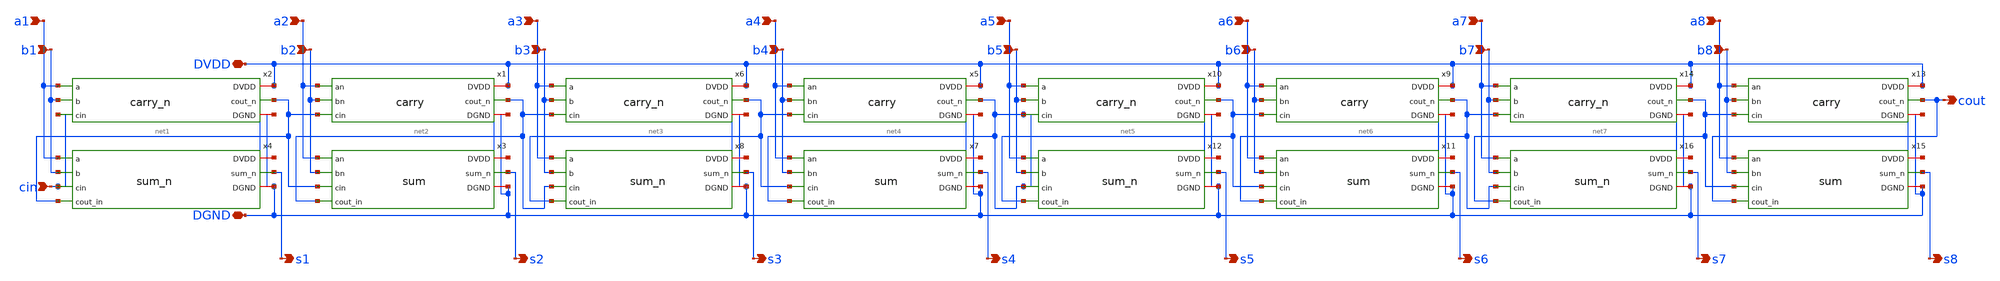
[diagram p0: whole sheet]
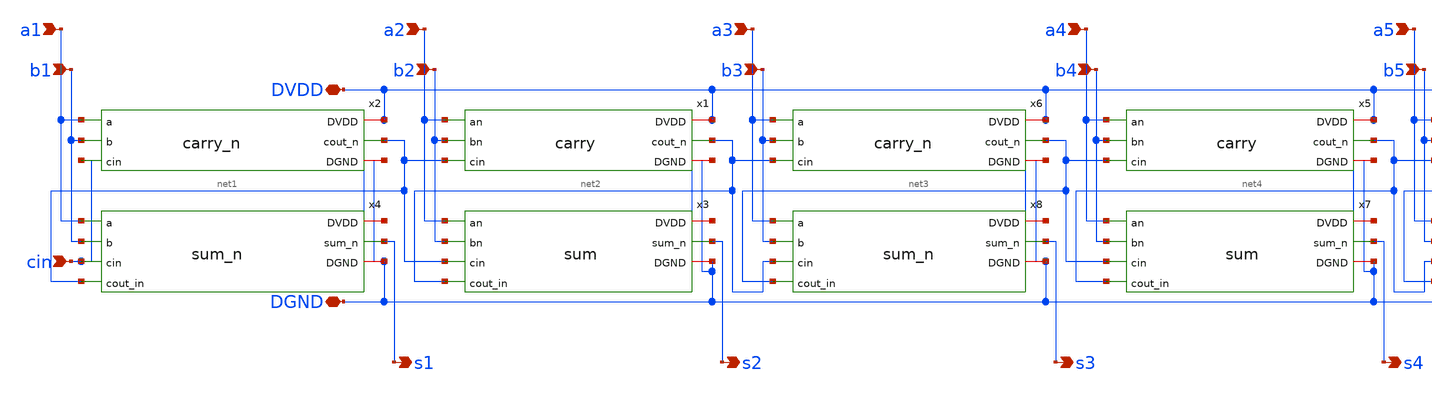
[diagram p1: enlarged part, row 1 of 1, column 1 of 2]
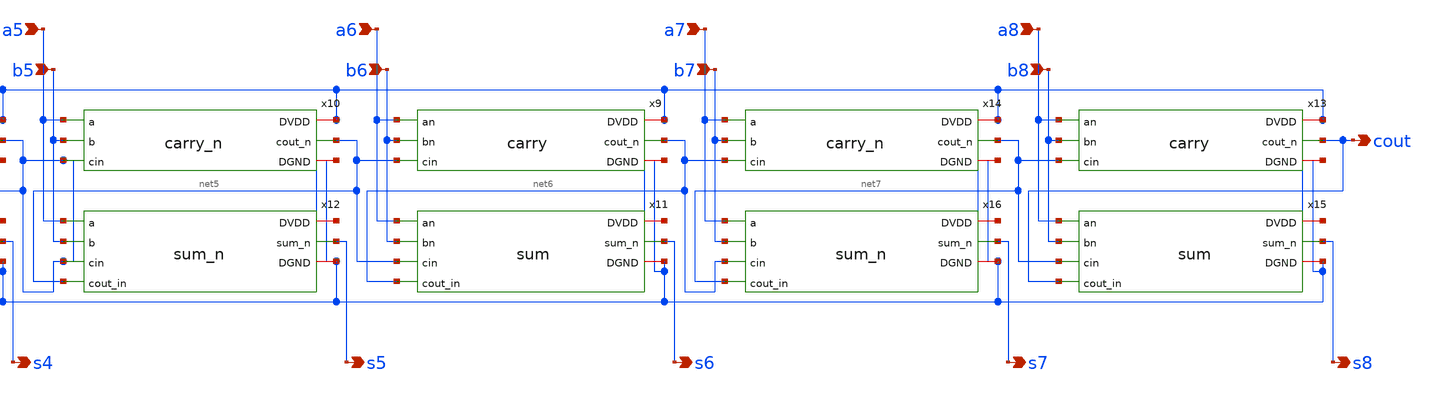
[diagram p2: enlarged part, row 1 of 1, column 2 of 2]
** sch_path: tut6/rca/rca8b.sch
**.subckt rca8b cin a1 b1 a2 b2 a3 b3 a4 b4 a5 b5 a6 b6 a7 b7 a8 b8 DVDD DGND s1 s2 s3 s4 s5 s6 s7
*+ s8 cout
*.ipin cin
*.ipin a1
*.ipin b1
*.ipin a2
*.ipin b2
*.ipin a3
*.ipin b3
*.ipin a4
*.ipin b4
*.ipin a5
*.ipin b5
*.ipin a6
*.ipin b6
*.ipin a7
*.ipin b7
*.ipin a8
*.ipin b8
*.iopin DVDD
*.iopin DGND
*.opin s1
*.opin s2
*.opin s3
*.opin s4
*.opin s5
*.opin s6
*.opin s7
*.opin s8
*.opin cout
x1 DVDD a2 b2 net2 net1 DGND carry
x2 DVDD a1 b1 net1 cin DGND carry_n
x3 DVDD a2 s2 b2 net1 net2 DGND sum
x4 DVDD a1 b1 s1 cin net1 DGND sum_n
x5 DVDD a4 b4 net4 net3 DGND carry
x6 DVDD a3 b3 net3 net2 DGND carry_n
x7 DVDD a4 s4 b4 net3 net4 DGND sum
x8 DVDD a3 b3 s3 net2 net3 DGND sum_n
x9 DVDD a6 b6 net6 net5 DGND carry
x10 DVDD a5 b5 net5 net4 DGND carry_n
x11 DVDD a6 s6 b6 net5 net6 DGND sum
x12 DVDD a5 b5 s5 net4 net5 DGND sum_n
x13 DVDD a8 b8 cout net7 DGND carry
x14 DVDD a7 b7 net7 net6 DGND carry_n
x15 DVDD a8 s8 b8 net7 cout DGND sum
x16 DVDD a7 b7 s7 net6 net7 DGND sum_n
**.ends
.end
